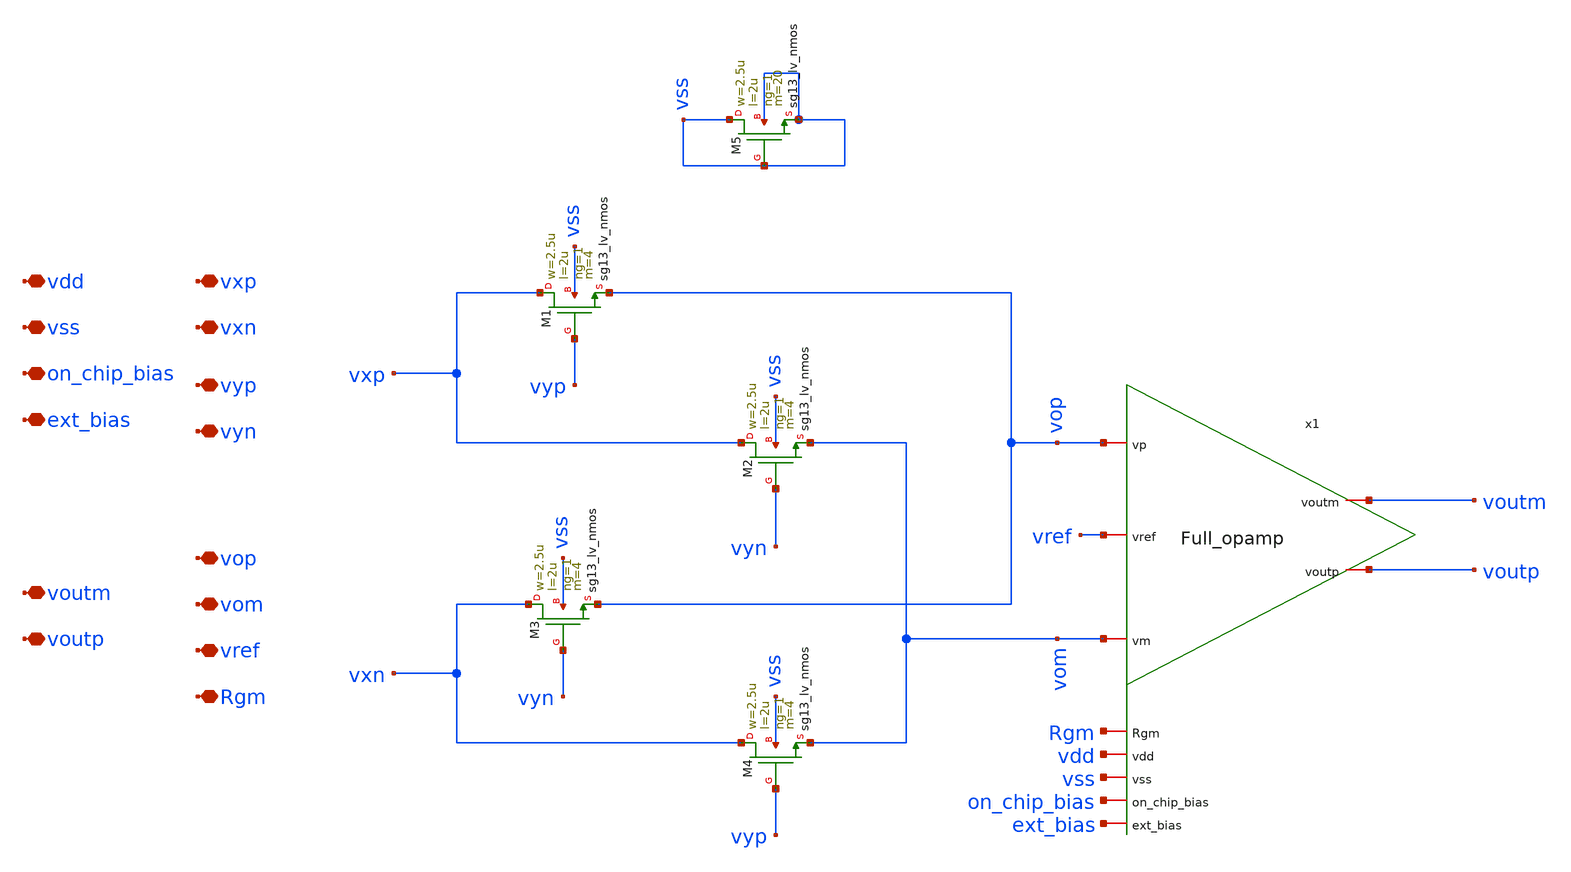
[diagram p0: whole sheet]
** sch_path: LVS/Unic_cass_final_design_lvs/Simulations/Multiplier/Src/multiplier.sch
**.subckt multiplier vxp vxn vyp vyn vop vom vref Rgm vdd vss on_chip_bias ext_bias voutm voutp
*.iopin vxp
*.iopin vxn
*.iopin vyp
*.iopin vyn
*.iopin vop
*.iopin vom
*.iopin vref
*.iopin Rgm
*.iopin vdd
*.iopin vss
*.iopin on_chip_bias
*.iopin ext_bias
*.iopin voutm
*.iopin voutp
x1 on_chip_bias vref vdd voutm ext_bias vom voutp vss vop Rgm Full_opamp
XM1 vxp vyp vop vss sg13_lv_nmos w=2.5u l=2u ng=1 m=4 mm_ok=1
XM2 vxp vyn vom vss sg13_lv_nmos w=2.5u l=2u ng=1 m=4 mm_ok=1
XM3 vxn vyn vop vss sg13_lv_nmos w=2.5u l=2u ng=1 m=4 mm_ok=1
XM4 vxn vyp vom vss sg13_lv_nmos w=2.5u l=2u ng=1 m=4 mm_ok=1
XM5 vss vss vss vss sg13_lv_nmos w=2.5u l=2u ng=1 m=20 mm_ok=1
**.ends
.end
